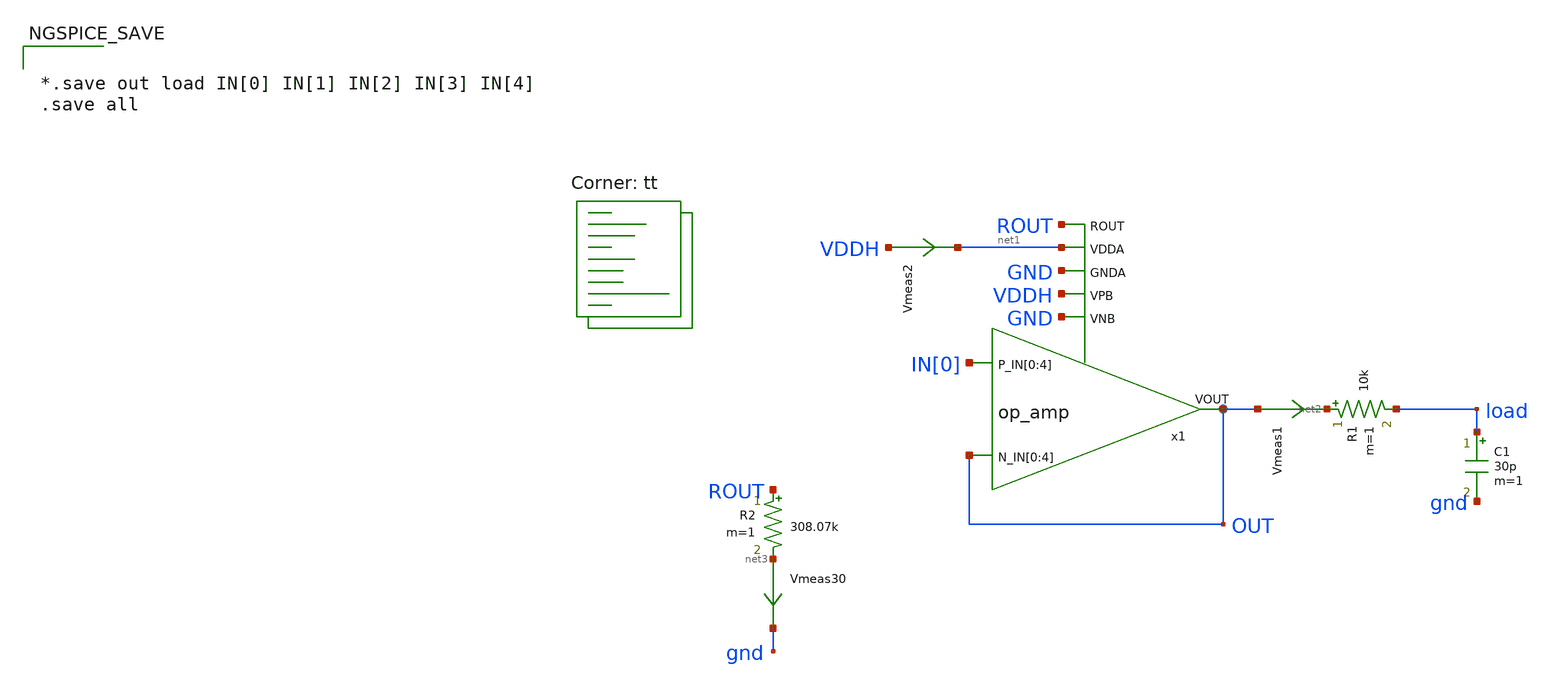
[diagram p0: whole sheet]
** sch_path: xschem/op_amp_top-tb.sch
**.subckt op_amp_top-tb
C1 load gnd 30p m=1
R1 net2 load 10k m=1
x1 IN[0] IN[0] IN[0] IN[0] IN[0] OUT OUT OUT OUT OUT OUT ROUT net1 GND VDDH GND op_amp
Vmeas1 OUT net2 0
.save i(vmeas1)
R2 ROUT net3 308.07k m=1
Vmeas30 net3 gnd 0
.save i(vmeas30)
Vmeas2 VDDH net1 0
.save i(vmeas2)
**** begin user architecture code



  .option wnflag=1
  .option safecurrents
  ********************Static Voltage Sources***************************
  Vddh vddh gnd dc 5.5
  ********************Dynamic Voltage Sources***************************
  *******Calculation**********
  .param base_f=100e3 base_t={1/base_f} base_th={base_t/2} base_d={base_th}
  .param b0_th={base_th} b0_t={b0_th*2}
  .param b1_th={b0_th*2} b1_t={b1_th*2}
  .param b2_th={b1_th*2} b2_t={b2_th*2}
  .param b3_th={b2_th*2} b3_t={b3_th*2}
  *******Signals**********
  .param vh=1.162 vl=1.044
  *vin0 in[0] gnd dc pulse(5.5 0 {base_d} 1n 1n {b0_th} {b0_t})
  vin0 in[0] gnd dc vl
  Vin1 in[1] gnd pulse({vh} {vl} {base_d} 1n 1n {b0_th} {b0_t})
  Vin2 in[2] gnd pulse({vh} {vl} {base_d} 1n 1n {b1_th} {b1_t})
  Vin3 in[3] gnd pulse({vh} {vl} {base_d} 1n 1n {b2_th} {b2_t})
  Vin4 in[4] gnd pulse({vh} {vl} {base_d} 1n 1n {b3_th} {b3_t})
  ********************Simulation Commands*****************************
  .control
     reset
     op
     write op_amp_top-tb.raw


     *tran 1n 100u
     dc vin0 -1 6.5 0.01
     *ac dec 100 1 1e9

     let vout_mag =abs(v(out))
     let vout_phase_margin = phase(v(out))*180/pi + 180
     meas ac Aol find vout_mag at = 10
     meas ac UGF when vout_mag=1 fall=1
     meas ac PM find vout_phase_margin when vout_mag=1
     let difference = v(inc) - v(ind)
     save difference
     write op_amp_top-tb.raw

     set wr_vecnames
     set wr_singlescale
     wrdata /home/yohanes/10-bit-DAC/simulations/op_amp_top-tb.txt out load
*    quit 0
  .endc





*.save out load IN[0] IN[1] IN[2] IN[3] IN[4]
.save all


.lib $::SKYWATER_MODELS/sky130.lib.spice tt
**** end user architecture code
**.ends

* expanding   symbol:  op_amp.sym # of pins=8
** sym_path: xschem/op_amp.sym
** sch_path: xschem/op_amp.sch
.subckt op_amp P_IN[0] P_IN[1] P_IN[2] P_IN[3] P_IN[4] N_IN[0] N_IN[1] N_IN[2] N_IN[3] N_IN[4] VOUT
+ ROUT VDDA GNDA VPB VNB
*.ipin P_IN[0],P_IN[1],P_IN[2],P_IN[3],P_IN[4]
*.ipin ROUT
*.opin VOUT
*.ipin VDDA
*.ipin VPB
*.ipin GNDA
*.ipin VNB
*.ipin N_IN[0],N_IN[1],N_IN[2],N_IN[3],N_IN[4]
x7 VHEAD1 VHEAD2 I_HEAD0 VDDA VPB head m=2
x8 VHEAD1 VHEAD2 I_HEAD1 VDDA VPB head m=2
x9 VHEAD1 VHEAD2 I_HEAD2 VDDA VPB head m=4
x10 VHEAD1 VHEAD2 I_HEAD3 VDDA VPB head m=8
x11 VHEAD1 VHEAD2 I_HEAD4 VDDA VPB head m=16
x12 VTAIL1 VTAIL2 I_TAIL0 GNDA VNB tail mv=2
x13 VTAIL1 VTAIL2 I_TAIL1 GNDA VNB tail mv=2
x14 VTAIL1 VTAIL2 I_TAIL2 GNDA VNB tail mv=4
x15 VTAIL1 VTAIL2 I_TAIL3 GNDA VNB tail mv=8
x16 VTAIL1 VTAIL2 I_TAIL4 GNDA VNB tail mv=16
x6 VHEAD2 VTAIL2 VBS1 VBS2 I_OPA I_OPB I_ONA I_ONB GP GN VDDA GNDA VPB VNB folded_cascode
x4 P_IN[1] N_IN[1] I_OPA I_OPB I_ONA I_ONB I_HEAD1 I_TAIL1 VPB VNB diff_pair
x5 P_IN[0] N_IN[0] I_OPA I_OPB I_ONA I_ONB I_HEAD0 I_TAIL0 VPB VNB diff_pair
x17 GP GN VOUT VDDA GNDA VPB VNB output_stage
x18 ROUT VHEAD1 VHEAD2 VTAIL1 VTAIL2 VBS1 VBS2 VDDA GNDA VPB VNB bias_opamp
x1 P_IN[3] N_IN[3] I_OPA I_OPB I_ONA I_ONB I_HEAD3 I_TAIL3 VPB VNB diff_pair
x2 P_IN[2] N_IN[2] I_OPA I_OPB I_ONA I_ONB I_HEAD2 I_TAIL2 VPB VNB diff_pair
x3 P_IN[4] N_IN[4] I_OPA I_OPB I_ONA I_ONB I_HEAD4 I_TAIL4 VPB VNB diff_pair
XC2 I_ONA VOUT sky130_fd_pr__cap_mim_m3_1 W=2 L=2 MF=20 m=20
XC3 I_OPA VOUT sky130_fd_pr__cap_mim_m3_1 W=2 L=2 MF=20 m=20
.ends


* expanding   symbol:  head.sym # of pins=5
** sym_path: xschem/head.sym
** sch_path: xschem/head.sch
.subckt head VB1 VB2 I_OUT VDDA VPB
*.opin I_OUT
*.ipin VB1
*.ipin VB2
*.ipin VDDA
*.ipin VPB
XM1 n1 VB1 VDDA VPB sky130_fd_pr__pfet_g5v0d10v5 L=10 W=1.8 nf=1 ad='int((nf+1)/2) * W/nf * 0.29' as='int((nf+2)/2) * W/nf * 0.29'
+ pd='2*int((nf+1)/2) * (W/nf + 0.29)' ps='2*int((nf+2)/2) * (W/nf + 0.29)' nrd='0.29 / W' nrs='0.29 / W'
+ sa=0 sb=0 sd=0 mult=m m=m
.param wp_iref=1.8 liref=10

Vmeas net1 I_OUT 0
.save i(vmeas)
XM2 net1 VB2 n1 VPB sky130_fd_pr__pfet_g5v0d10v5 L=10 W=1.8 nf=1 ad='int((nf+1)/2) * W/nf * 0.29' as='int((nf+2)/2) * W/nf * 0.29'
+ pd='2*int((nf+1)/2) * (W/nf + 0.29)' ps='2*int((nf+2)/2) * (W/nf + 0.29)' nrd='0.29 / W' nrs='0.29 / W'
+ sa=0 sb=0 sd=0 mult=m m=m
.ends


* expanding   symbol:  tail.sym # of pins=5
** sym_path: xschem/tail.sym
** sch_path: xschem/tail.sch
.subckt tail VB1 VB2 I_OUT GNDA VNB  mv=1
*.opin I_OUT
*.ipin VB1
*.ipin VB2
*.ipin GNDA
*.ipin VNB
.param wn_iref=0.6 liref=10

XM1 net1 VB2 n1 VNB sky130_fd_pr__nfet_g5v0d10v5 L=10 W=0.6 nf=1 ad='int((nf+1)/2) * W/nf * 0.29' as='int((nf+2)/2) * W/nf * 0.29'
+ pd='2*int((nf+1)/2) * (W/nf + 0.29)' ps='2*int((nf+2)/2) * (W/nf + 0.29)' nrd='0.29 / W' nrs='0.29 / W'
+ sa=0 sb=0 sd=0 mult=mv m=mv
Vmeas I_OUT net1 0
.save i(vmeas)
XM2 n1 VB1 GNDA VNB sky130_fd_pr__nfet_g5v0d10v5 L=10 W=0.6 nf=1 ad='int((nf+1)/2) * W/nf * 0.29' as='int((nf+2)/2) * W/nf * 0.29'
+ pd='2*int((nf+1)/2) * (W/nf + 0.29)' ps='2*int((nf+2)/2) * (W/nf + 0.29)' nrd='0.29 / W' nrs='0.29 / W'
+ sa=0 sb=0 sd=0 mult=mv m=mv
.ends


* expanding   symbol:  folded_cascode.sym # of pins=14
** sym_path: xschem/folded_cascode.sym
** sch_path: xschem/folded_cascode.sch
.subckt folded_cascode VBS1 VBS2 VB1 VB2 I_OPA I_OPB I_ONA I_ONB OUTA OUTB VDDA GNDA VPB VNB
*.ipin I_OPA
*.ipin I_OPB
*.ipin I_ONA
*.ipin I_ONB
*.opin OUTA
*.opin OUTB
*.ipin VBS1
*.ipin VBS2
*.ipin VB1
*.ipin VB2
*.ipin VDDA
*.ipin VPB
*.ipin GNDA
*.ipin VNB
.param wp_sum=4.8 wn_sum=1.6 l_sum=1 m_sum=2 wp_fcm=4.8 wn_fcm=1.6 m_fcm=2

XM3 I_ONB VGP net1 VPB sky130_fd_pr__pfet_g5v0d10v5 L=l_sum W=wp_sum nf=1 ad='int((nf+1)/2) * W/nf * 0.29'
+ as='int((nf+2)/2) * W/nf * 0.29' pd='2*int((nf+1)/2) * (W/nf + 0.29)' ps='2*int((nf+2)/2) * (W/nf + 0.29)'
+ nrd='0.29 / W' nrs='0.29 / W' sa=0 sb=0 sd=0 mult=m_sum m=m_sum
Vmeas1 VDDA net1 0
.save i(vmeas1)
Vmeas2 VDDA net2 0
.save i(vmeas2)
XM7 net3 VB2 OUTB VNB sky130_fd_pr__nfet_g5v0d10v5 L=l_sum W=wn_fcm nf=1 ad='int((nf+1)/2) * W/nf * 0.29'
+ as='int((nf+2)/2) * W/nf * 0.29' pd='2*int((nf+1)/2) * (W/nf + 0.29)' ps='2*int((nf+2)/2) * (W/nf + 0.29)'
+ nrd='0.29 / W' nrs='0.29 / W' sa=0 sb=0 sd=0 mult=m_fcm m=m_fcm
XM8 net4 VB2 VGN VNB sky130_fd_pr__nfet_g5v0d10v5 L=l_sum W=wn_fcm nf=1 ad='int((nf+1)/2) * W/nf * 0.29'
+ as='int((nf+2)/2) * W/nf * 0.29' pd='2*int((nf+1)/2) * (W/nf + 0.29)' ps='2*int((nf+2)/2) * (W/nf + 0.29)'
+ nrd='0.29 / W' nrs='0.29 / W' sa=0 sb=0 sd=0 mult=m_fcm m=m_fcm
Vmeas3 VGP net4 0
.save i(vmeas3)
Vmeas4 OUTA net3 0
.save i(vmeas4)
XM10 VGN VB1 net5 VPB sky130_fd_pr__pfet_g5v0d10v5 L=l_sum W=wp_fcm nf=1 ad='int((nf+1)/2) * W/nf * 0.29'
+ as='int((nf+2)/2) * W/nf * 0.29' pd='2*int((nf+1)/2) * (W/nf + 0.29)' ps='2*int((nf+2)/2) * (W/nf + 0.29)'
+ nrd='0.29 / W' nrs='0.29 / W' sa=0 sb=0 sd=0 mult=m_fcm m=m_fcm
Vmeas5 VGP net5 0
.save i(vmeas5)
Vmeas6 OUTA net6 0
.save i(vmeas6)
XM9 OUTB VB1 net6 VPB sky130_fd_pr__pfet_g5v0d10v5 L=l_sum W=wp_fcm nf=1 ad='int((nf+1)/2) * W/nf * 0.29'
+ as='int((nf+2)/2) * W/nf * 0.29' pd='2*int((nf+1)/2) * (W/nf + 0.29)' ps='2*int((nf+2)/2) * (W/nf + 0.29)'
+ nrd='0.29 / W' nrs='0.29 / W' sa=0 sb=0 sd=0 mult=m_fcm m=m_fcm
XM12 net7 VBS2 I_OPB VNB sky130_fd_pr__nfet_g5v0d10v5 L=l_sum W=wn_sum nf=1 ad='int((nf+1)/2) * W/nf * 0.29'
+ as='int((nf+2)/2) * W/nf * 0.29' pd='2*int((nf+1)/2) * (W/nf + 0.29)' ps='2*int((nf+2)/2) * (W/nf + 0.29)'
+ nrd='0.29 / W' nrs='0.29 / W' sa=0 sb=0 sd=0 mult=m_sum m=m_sum
Vmeas7 VGN net7 0
.save i(vmeas7)
Vmeas8 OUTB net8 0
.save i(vmeas8)
XM11 net8 VBS2 I_OPA VNB sky130_fd_pr__nfet_g5v0d10v5 L=l_sum W=wn_sum nf=1 ad='int((nf+1)/2) * W/nf * 0.29'
+ as='int((nf+2)/2) * W/nf * 0.29' pd='2*int((nf+1)/2) * (W/nf + 0.29)' ps='2*int((nf+2)/2) * (W/nf + 0.29)'
+ nrd='0.29 / W' nrs='0.29 / W' sa=0 sb=0 sd=0 mult=m_sum m=m_sum
XM13 I_OPB VGN net9 VNB sky130_fd_pr__nfet_g5v0d10v5 L=l_sum W={wn_sum*3} nf=1 ad='int((nf+1)/2) * W/nf * 0.29'
+ as='int((nf+2)/2) * W/nf * 0.29' pd='2*int((nf+1)/2) * (W/nf + 0.29)' ps='2*int((nf+2)/2) * (W/nf + 0.29)'
+ nrd='0.29 / W' nrs='0.29 / W' sa=0 sb=0 sd=0 mult=m_sum m=m_sum
Vmeas9 net9 GNDA 0
.save i(vmeas9)
Vmeas10 net10 GNDA 0
.save i(vmeas10)
XM14 I_OPA VGN net10 VNB sky130_fd_pr__nfet_g5v0d10v5 L=l_sum W={wn_sum*3} nf=1 ad='int((nf+1)/2) * W/nf * 0.29'
+ as='int((nf+2)/2) * W/nf * 0.29' pd='2*int((nf+1)/2) * (W/nf + 0.29)' ps='2*int((nf+2)/2) * (W/nf + 0.29)'
+ nrd='0.29 / W' nrs='0.29 / W' sa=0 sb=0 sd=0 mult=m_sum m=m_sum
XM1 VGP VBS1 I_ONB VPB sky130_fd_pr__pfet_g5v0d10v5 L=l_sum W=wp_sum nf=1 ad='int((nf+1)/2) * W/nf * 0.29'
+ as='int((nf+2)/2) * W/nf * 0.29' pd='2*int((nf+1)/2) * (W/nf + 0.29)' ps='2*int((nf+2)/2) * (W/nf + 0.29)'
+ nrd='0.29 / W' nrs='0.29 / W' sa=0 sb=0 sd=0 mult=m_sum m=m_sum
XM2 I_ONA VGP net2 VPB sky130_fd_pr__pfet_g5v0d10v5 L=l_sum W=wp_sum nf=1 ad='int((nf+1)/2) * W/nf * 0.29'
+ as='int((nf+2)/2) * W/nf * 0.29' pd='2*int((nf+1)/2) * (W/nf + 0.29)' ps='2*int((nf+2)/2) * (W/nf + 0.29)'
+ nrd='0.29 / W' nrs='0.29 / W' sa=0 sb=0 sd=0 mult=m_sum m=m_sum
XM4 OUTA VBS1 I_ONA VPB sky130_fd_pr__pfet_g5v0d10v5 L=l_sum W=wp_sum nf=1 ad='int((nf+1)/2) * W/nf * 0.29'
+ as='int((nf+2)/2) * W/nf * 0.29' pd='2*int((nf+1)/2) * (W/nf + 0.29)' ps='2*int((nf+2)/2) * (W/nf + 0.29)'
+ nrd='0.29 / W' nrs='0.29 / W' sa=0 sb=0 sd=0 mult=m_sum m=m_sum
.ends


* expanding   symbol:  diff_pair.sym # of pins=10
** sym_path: xschem/diff_pair.sym
** sch_path: xschem/diff_pair.sch
.subckt diff_pair P_IN N_IN I_OPA I_OPB I_ONA I_ONB I_HEAD I_TAIL VPB VNB  weight=1
*.opin I_OPA
*.opin I_OPB
*.ipin P_IN
*.ipin N_IN
*.opin I_ONA
*.opin I_ONB
*.ipin I_HEAD
*.ipin I_TAIL
*.ipin VPB
*.ipin VNB
XM1 I_OPA P_IN I_HEAD VPB sky130_fd_pr__pfet_g5v0d10v5 L=l_diff W=wp_diff nf=1 ad='int((nf+1)/2) * W/nf * 0.29'
+ as='int((nf+2)/2) * W/nf * 0.29' pd='2*int((nf+1)/2) * (W/nf + 0.29)' ps='2*int((nf+2)/2) * (W/nf + 0.29)'
+ nrd='0.29 / W' nrs='0.29 / W' sa=0 sb=0 sd=0 mult=2 m=2
XM3 I_ONA P_IN I_TAIL VNB sky130_fd_pr__nfet_g5v0d10v5 L=l_diff W=wn_diff nf=1 ad='int((nf+1)/2) * W/nf * 0.29'
+ as='int((nf+2)/2) * W/nf * 0.29' pd='2*int((nf+1)/2) * (W/nf + 0.29)' ps='2*int((nf+2)/2) * (W/nf + 0.29)'
+ nrd='0.29 / W' nrs='0.29 / W' sa=0 sb=0 sd=0 mult=2 m=2
.param wp_diff=3 wn_diff=1 l_diff=1

XM2 I_OPB N_IN I_HEAD VPB sky130_fd_pr__pfet_g5v0d10v5 L=l_diff W=wp_diff nf=1 ad='int((nf+1)/2) * W/nf * 0.29'
+ as='int((nf+2)/2) * W/nf * 0.29' pd='2*int((nf+1)/2) * (W/nf + 0.29)' ps='2*int((nf+2)/2) * (W/nf + 0.29)'
+ nrd='0.29 / W' nrs='0.29 / W' sa=0 sb=0 sd=0 mult=2 m=2
XM4 I_ONB N_IN I_TAIL VNB sky130_fd_pr__nfet_g5v0d10v5 L=l_diff W=wn_diff nf=1 ad='int((nf+1)/2) * W/nf * 0.29'
+ as='int((nf+2)/2) * W/nf * 0.29' pd='2*int((nf+1)/2) * (W/nf + 0.29)' ps='2*int((nf+2)/2) * (W/nf + 0.29)'
+ nrd='0.29 / W' nrs='0.29 / W' sa=0 sb=0 sd=0 mult=2 m=2
.ends


* expanding   symbol:  output_stage.sym # of pins=7
** sym_path: xschem/output_stage.sym
** sch_path: xschem/output_stage.sch
.subckt output_stage GP GN VOUT VDDA GNDA VPB VNB
*.ipin GP
*.ipin GN
*.opin VOUT
*.ipin VDDA
*.ipin VPB
*.ipin GNDA
*.ipin VNB
XM1 VOUT GP net1 VPB sky130_fd_pr__pfet_g5v0d10v5 L=1 W=6 nf=1 ad='int((nf+1)/2) * W/nf * 0.29' as='int((nf+2)/2) * W/nf * 0.29'
+ pd='2*int((nf+1)/2) * (W/nf + 0.29)' ps='2*int((nf+2)/2) * (W/nf + 0.29)' nrd='0.29 / W' nrs='0.29 / W'
+ sa=0 sb=0 sd=0 mult=2 m=2
XM2 VOUT GN net2 VNB sky130_fd_pr__nfet_g5v0d10v5 L=1 W=2 nf=1 ad='int((nf+1)/2) * W/nf * 0.29' as='int((nf+2)/2) * W/nf * 0.29'
+ pd='2*int((nf+1)/2) * (W/nf + 0.29)' ps='2*int((nf+2)/2) * (W/nf + 0.29)' nrd='0.29 / W' nrs='0.29 / W'
+ sa=0 sb=0 sd=0 mult=2 m=2
Vmeas1 VDDA net1 0
.save i(vmeas1)
Vmeas2 net2 GNDA 0
.save i(vmeas2)
.ends


* expanding   symbol:  bias_opamp.sym # of pins=11
** sym_path: xschem/bias_opamp.sym
** sch_path: xschem/bias_opamp.sch
.subckt bias_opamp ROUT VHEAD1 VHEAD2 VTAIL1 VTAIL2 VBS1 VBS2 VDDA GNDA VPB VNB
*.ipin ROUT
*.opin VHEAD1
*.ipin VDDA
*.ipin VPB
*.ipin GNDA
*.ipin VNB
*.opin VHEAD2
*.opin VTAIL1
*.opin VTAIL2
*.opin VBS1
*.opin VBS2
XM1 net1 VHEAD1 VDDA VPB sky130_fd_pr__pfet_g5v0d10v5 L=lref W=wp_iref nf=1 ad='int((nf+1)/2) * W/nf * 0.29'
+ as='int((nf+2)/2) * W/nf * 0.29' pd='2*int((nf+1)/2) * (W/nf + 0.29)' ps='2*int((nf+2)/2) * (W/nf + 0.29)'
+ nrd='0.29 / W' nrs='0.29 / W' sa=0 sb=0 sd=0 mult=miref m=miref
XM2 VHEAD1 VHEAD2 net1 VPB sky130_fd_pr__pfet_g5v0d10v5 L=lref W=wp_iref nf=1 ad='int((nf+1)/2) * W/nf * 0.29'
+ as='int((nf+2)/2) * W/nf * 0.29' pd='2*int((nf+1)/2) * (W/nf + 0.29)' ps='2*int((nf+2)/2) * (W/nf + 0.29)'
+ nrd='0.29 / W' nrs='0.29 / W' sa=0 sb=0 sd=0 mult=miref m=miref
XM3 VHEAD2 net2 VHEAD1 VPB sky130_fd_pr__pfet_g5v0d10v5 L=lr W=wp_iref nf=1 ad='int((nf+1)/2) * W/nf * 0.29'
+ as='int((nf+2)/2) * W/nf * 0.29' pd='2*int((nf+1)/2) * (W/nf + 0.29)' ps='2*int((nf+2)/2) * (W/nf + 0.29)'
+ nrd='0.29 / W' nrs='0.29 / W' sa=0 sb=0 sd=0 mult=2 m=2
XM7 net6 VHEAD1 VDDA VPB sky130_fd_pr__pfet_g5v0d10v5 L=lref W=wp_iref nf=1 ad='int((nf+1)/2) * W/nf * 0.29'
+ as='int((nf+2)/2) * W/nf * 0.29' pd='2*int((nf+1)/2) * (W/nf + 0.29)' ps='2*int((nf+2)/2) * (W/nf + 0.29)'
+ nrd='0.29 / W' nrs='0.29 / W' sa=0 sb=0 sd=0 mult=miref m=miref
XM8 net5 VHEAD2 net6 VPB sky130_fd_pr__pfet_g5v0d10v5 L=lref W=wp_iref nf=1 ad='int((nf+1)/2) * W/nf * 0.29'
+ as='int((nf+2)/2) * W/nf * 0.29' pd='2*int((nf+1)/2) * (W/nf + 0.29)' ps='2*int((nf+2)/2) * (W/nf + 0.29)'
+ nrd='0.29 / W' nrs='0.29 / W' sa=0 sb=0 sd=0 mult=miref m=miref
XM4 net2 net2 VHEAD2 VPB sky130_fd_pr__pfet_g5v0d10v5 L=lr W=wp_iref nf=1 ad='int((nf+1)/2) * W/nf * 0.29'
+ as='int((nf+2)/2) * W/nf * 0.29' pd='2*int((nf+1)/2) * (W/nf + 0.29)' ps='2*int((nf+2)/2) * (W/nf + 0.29)'
+ nrd='0.29 / W' nrs='0.29 / W' sa=0 sb=0 sd=0 mult=2 m=2
XM5 net3 net9 net2 VPB sky130_fd_pr__pfet_g5v0d10v5 L=lr W=wp_iref nf=1 ad='int((nf+1)/2) * W/nf * 0.29'
+ as='int((nf+2)/2) * W/nf * 0.29' pd='2*int((nf+1)/2) * (W/nf + 0.29)' ps='2*int((nf+2)/2) * (W/nf + 0.29)'
+ nrd='0.29 / W' nrs='0.29 / W' sa=0 sb=0 sd=0 mult=2 m=2
XM6 net9 net9 net3 VPB sky130_fd_pr__pfet_g5v0d10v5 L=lr W=wp_iref nf=1 ad='int((nf+1)/2) * W/nf * 0.29'
+ as='int((nf+2)/2) * W/nf * 0.29' pd='2*int((nf+1)/2) * (W/nf + 0.29)' ps='2*int((nf+2)/2) * (W/nf + 0.29)'
+ nrd='0.29 / W' nrs='0.29 / W' sa=0 sb=0 sd=0 mult=2 m=2
XM9 net5 net5 VTAIL2 VNB sky130_fd_pr__nfet_g5v0d10v5 L=lr W=wn_iref nf=1 ad='int((nf+1)/2) * W/nf * 0.29'
+ as='int((nf+2)/2) * W/nf * 0.29' pd='2*int((nf+1)/2) * (W/nf + 0.29)' ps='2*int((nf+2)/2) * (W/nf + 0.29)'
+ nrd='0.29 / W' nrs='0.29 / W' sa=0 sb=0 sd=0 mult=2 m=2
XM10 VTAIL2 net5 VTAIL1 VNB sky130_fd_pr__nfet_g5v0d10v5 L=lr W=wn_iref nf=1 ad='int((nf+1)/2) * W/nf * 0.29'
+ as='int((nf+2)/2) * W/nf * 0.29' pd='2*int((nf+1)/2) * (W/nf + 0.29)' ps='2*int((nf+2)/2) * (W/nf + 0.29)'
+ nrd='0.29 / W' nrs='0.29 / W' sa=0 sb=0 sd=0 mult=2 m=2
XM11 VTAIL1 VTAIL2 net4 VNB sky130_fd_pr__nfet_g5v0d10v5 L=lref W=wn_iref nf=1 ad='int((nf+1)/2) * W/nf * 0.29'
+ as='int((nf+2)/2) * W/nf * 0.29' pd='2*int((nf+1)/2) * (W/nf + 0.29)' ps='2*int((nf+2)/2) * (W/nf + 0.29)'
+ nrd='0.29 / W' nrs='0.29 / W' sa=0 sb=0 sd=0 mult=miref m=miref
XM12 net4 VTAIL1 net10 VNB sky130_fd_pr__nfet_g5v0d10v5 L=lref W=wn_iref nf=1 ad='int((nf+1)/2) * W/nf * 0.29'
+ as='int((nf+2)/2) * W/nf * 0.29' pd='2*int((nf+1)/2) * (W/nf + 0.29)' ps='2*int((nf+2)/2) * (W/nf + 0.29)'
+ nrd='0.29 / W' nrs='0.29 / W' sa=0 sb=0 sd=0 mult=miref m=miref
.param wp_iref=1.8 wn_iref=0.6 miref=10 miref2=10 wp_bias=4.8 wn_bias=1.6 mbias=2 l=1 lref=10 lr=70
XM13 net7 VHEAD1 VDDA VPB sky130_fd_pr__pfet_g5v0d10v5 L=lref W=wp_iref nf=1 ad='int((nf+1)/2) * W/nf * 0.29'
+ as='int((nf+2)/2) * W/nf * 0.29' pd='2*int((nf+1)/2) * (W/nf + 0.29)' ps='2*int((nf+2)/2) * (W/nf + 0.29)'
+ nrd='0.29 / W' nrs='0.29 / W' sa=0 sb=0 sd=0 mult=miref2 m=miref2
XM14 VBS2 VHEAD2 net7 VPB sky130_fd_pr__pfet_g5v0d10v5 L=lref W=wp_iref nf=1 ad='int((nf+1)/2) * W/nf * 0.29'
+ as='int((nf+2)/2) * W/nf * 0.29' pd='2*int((nf+1)/2) * (W/nf + 0.29)' ps='2*int((nf+2)/2) * (W/nf + 0.29)'
+ nrd='0.29 / W' nrs='0.29 / W' sa=0 sb=0 sd=0 mult=miref2 m=miref2
XM15 VBS2 VBS2 NVB VNB sky130_fd_pr__nfet_g5v0d10v5 L=l W=wn_bias nf=1 ad='int((nf+1)/2) * W/nf * 0.29'
+ as='int((nf+2)/2) * W/nf * 0.29' pd='2*int((nf+1)/2) * (W/nf + 0.29)' ps='2*int((nf+2)/2) * (W/nf + 0.29)'
+ nrd='0.29 / W' nrs='0.29 / W' sa=0 sb=0 sd=0 mult=mbias m=mbias
XM17 PVB PVB VDDA VPB sky130_fd_pr__pfet_g5v0d10v5 L=l W=wp_bias nf=1 ad='int((nf+1)/2) * W/nf * 0.29'
+ as='int((nf+2)/2) * W/nf * 0.29' pd='2*int((nf+1)/2) * (W/nf + 0.29)' ps='2*int((nf+2)/2) * (W/nf + 0.29)'
+ nrd='0.29 / W' nrs='0.29 / W' sa=0 sb=0 sd=0 mult=mbias m=mbias
XM19 VBS1 VTAIL2 net8 VNB sky130_fd_pr__nfet_g5v0d10v5 L=lref W=wn_iref nf=1 ad='int((nf+1)/2) * W/nf * 0.29'
+ as='int((nf+2)/2) * W/nf * 0.29' pd='2*int((nf+1)/2) * (W/nf + 0.29)' ps='2*int((nf+2)/2) * (W/nf + 0.29)'
+ nrd='0.29 / W' nrs='0.29 / W' sa=0 sb=0 sd=0 mult=miref2 m=miref2
XM20 net8 VTAIL1 net11 VNB sky130_fd_pr__nfet_g5v0d10v5 L=lref W=wn_iref nf=1 ad='int((nf+1)/2) * W/nf * 0.29'
+ as='int((nf+2)/2) * W/nf * 0.29' pd='2*int((nf+1)/2) * (W/nf + 0.29)' ps='2*int((nf+2)/2) * (W/nf + 0.29)'
+ nrd='0.29 / W' nrs='0.29 / W' sa=0 sb=0 sd=0 mult=miref2 m=miref2
XR1 ROUT net9 GNDA sky130_fd_pr__res_xhigh_po_5p73 L=0.573 mult=1 m=1
XM18 VBS1 VBS1 PVB VPB sky130_fd_pr__pfet_g5v0d10v5 L=l W=wp_bias nf=1 ad='int((nf+1)/2) * W/nf * 0.29'
+ as='int((nf+2)/2) * W/nf * 0.29' pd='2*int((nf+1)/2) * (W/nf + 0.29)' ps='2*int((nf+2)/2) * (W/nf + 0.29)'
+ nrd='0.29 / W' nrs='0.29 / W' sa=0 sb=0 sd=0 mult=mbias m=mbias
XM16 NVB NVB net12 VNB sky130_fd_pr__nfet_g5v0d10v5 L=l W=wn_bias nf=1 ad='int((nf+1)/2) * W/nf * 0.29'
+ as='int((nf+2)/2) * W/nf * 0.29' pd='2*int((nf+1)/2) * (W/nf + 0.29)' ps='2*int((nf+2)/2) * (W/nf + 0.29)'
+ nrd='0.29 / W' nrs='0.29 / W' sa=0 sb=0 sd=0 mult=mbias m=mbias
Vmeas net10 GNDA 0
.save i(vmeas)
Vmeas1 net12 GNDA 0
.save i(vmeas1)
Vmeas2 net11 GNDA 0
.save i(vmeas2)
.ends

.end
